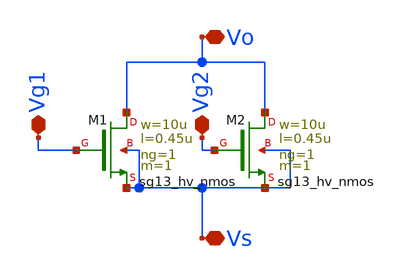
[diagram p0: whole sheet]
** sch_path: schematics/DCDCBuck_vto1p1_izquierdo.sch
**.subckt DCDCBuck_vto1p1_izquierdo Vs Vg1 Vg2 Vo
*.iopin Vs
*.iopin Vg1
*.iopin Vg2
*.iopin Vo
MM2 Vo Vg2 Vs Vs sg13_hv_nmos w=10u l=0.45u ng=1 m=1 mm_ok=1
MM1 Vo Vg1 Vs Vs sg13_hv_nmos w=10u l=0.45u ng=1 m=1 mm_ok=1
**.ends
.end
